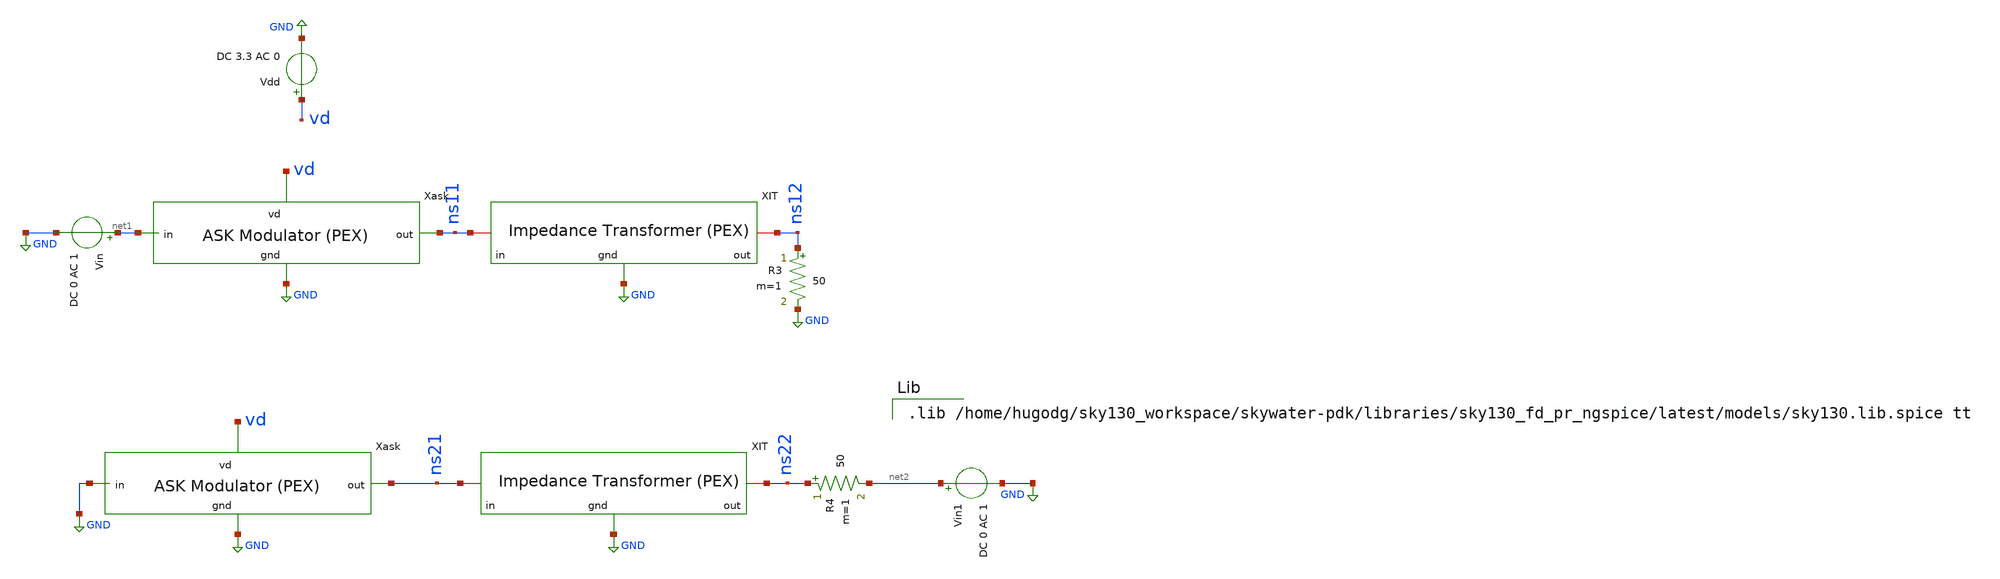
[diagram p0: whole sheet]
** sch_path: impedance-transformer/xschem/impedance-transformer-pex_tb-ac.sch
**.subckt impedance-transformer-pex_tb-ac
Vin net1 GND DC 0 AC 1
Vin1 net2 GND DC 0 AC 1
R3 ns12 GND 50 m=1
R4 ns22 net2 50 m=1
Vdd vd GND DC 3.3 AC 0
xask1 vd ns11 net1 GND ask-modulator-pex
xask2 vd ns21 GND GND ask-modulator-pex
xit1 ns11 ns12 GND impedance-transformer-pex
xit2 ns21 ns22 GND impedance-transformer-pex
**** begin user architecture code



.ac lin 1MEG 2G 4G
.control
destroy all
set units=degrees
run

set color0=white
set color1=black

let z0=50
let zl=169

* Find two S parameters from test circuit
let s11 = v(ns11)
let s12 = v(ns12)
let s21 = v(ns21)
let s22 = v(ns22)

* Extract Y parameters
*let StoYDelS = ((1+s11)*(1+s22)-s12*s21)*z0
*let y11 = ((1+s22)*(1-s11)+s12*s21/StoYDelS
*let y12=-2*s12/StoYDelS
*let y21=-2*s21/StoYDelS
*let y22 = ((1+s11)*(1-s22)+s12+s21)/StoYDelS

* Extract Z parameters
let StoZDelS = ((1-s11)*(1-s22)-s12*s21)/z0
let z11 = ((1+s11)*(1-s22)+s12*s21)/StoZDelS
let z12 = 2*s12/StoZDelS
let z21 = 2*s21/StoZDelS
let z22=((1-s11)*(1+s22)+s12*s21)/StoZDelS

*plot z11
*plot z12
*plot z21
plot z22 xlimit 2.4G 2.5G
plot ph(z22) xlimit 2.4G 2.5G
plot z22
*plot smith z22
let z_output= z22-(z12*z21/(z11+zl))
plot z_output
plot ph(z_output)
let z_in = z11-z12*z21/(z22+z0)
.endc


.lib /home/hugodg/sky130_workspace/skywater-pdk/libraries/sky130_fd_pr_ngspice/latest/models/sky130.lib.spice tt

**** end user architecture code
**.ends
.GLOBAL GND
.end
